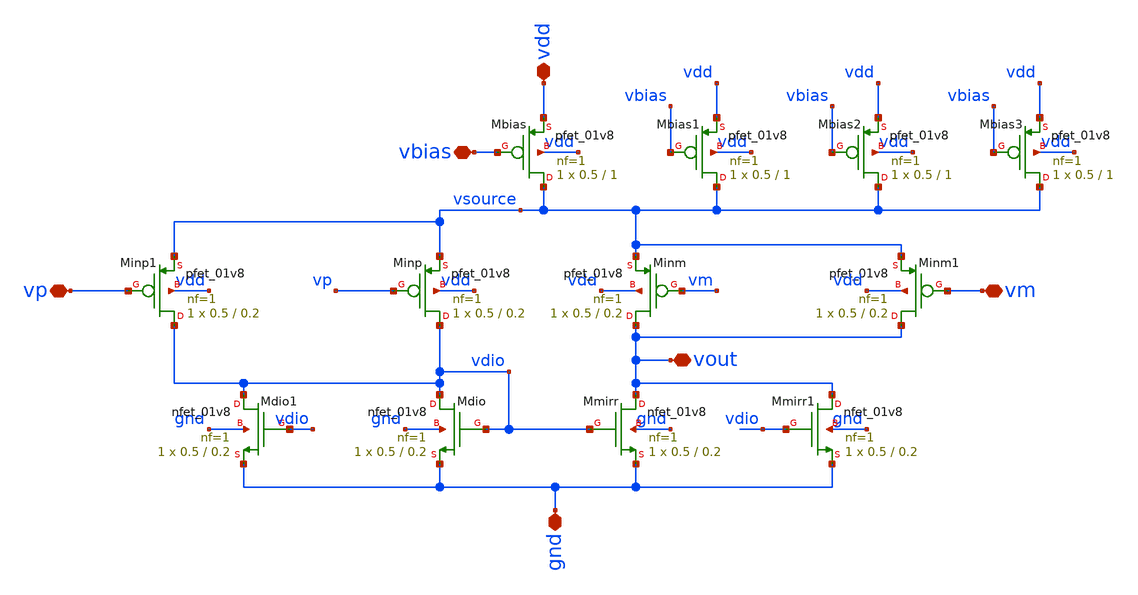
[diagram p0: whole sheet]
** sch_path: analog/xschem/final/col_amp_n_clamp_v1/amp_p_5T.sch
**.subckt amp_p_5T gnd vdd vout vbias vm vp
*.iopin gnd
*.iopin vdd
*.iopin vout
*.iopin vbias
*.iopin vm
*.iopin vp
XMinm vout vm vsource vdd sky130_fd_pr__pfet_01v8 L=0.2 W=0.5 nf=1 ad='int((1 + 1)/2) * 0.5 / 1 * 0.29'
+ as='int((1 + 2)/2) * 0.5 / 1 * 0.29' pd='2*int((1 + 1)/2) * (0.5 / 1 + 0.29)' ps='2*int((1 + 2)/2) * (0.5 / 1 + 0.29)'
+ nrd='0.29 / 0.5 ' nrs='0.29 / 0.5 ' sa=0 sb=0 sd=0 mult=1 m=1
XMinp vdio vp vsource vdd sky130_fd_pr__pfet_01v8 L=0.2 W=0.5 nf=1 ad='int((1 + 1)/2) * 0.5 / 1 * 0.29'
+ as='int((1 + 2)/2) * 0.5 / 1 * 0.29' pd='2*int((1 + 1)/2) * (0.5 / 1 + 0.29)' ps='2*int((1 + 2)/2) * (0.5 / 1 + 0.29)'
+ nrd='0.29 / 0.5 ' nrs='0.29 / 0.5 ' sa=0 sb=0 sd=0 mult=1 m=1
XMdio vdio vdio gnd gnd sky130_fd_pr__nfet_01v8 L=0.2 W=0.5 nf=1 ad='int((1 + 1)/2) * 0.5 / 1 * 0.29'
+ as='int((1 + 2)/2) * 0.5 / 1 * 0.29' pd='2*int((1 + 1)/2) * (0.5 / 1 + 0.29)' ps='2*int((1 + 2)/2) * (0.5 / 1 + 0.29)'
+ nrd='0.29 / 0.5 ' nrs='0.29 / 0.5 ' sa=0 sb=0 sd=0 mult=1 m=1
XMmirr vout vdio gnd gnd sky130_fd_pr__nfet_01v8 L=0.2 W=0.5 nf=1 ad='int((1 + 1)/2) * 0.5 / 1 * 0.29'
+ as='int((1 + 2)/2) * 0.5 / 1 * 0.29' pd='2*int((1 + 1)/2) * (0.5 / 1 + 0.29)' ps='2*int((1 + 2)/2) * (0.5 / 1 + 0.29)'
+ nrd='0.29 / 0.5 ' nrs='0.29 / 0.5 ' sa=0 sb=0 sd=0 mult=1 m=1
XMbias vsource vbias vdd vdd sky130_fd_pr__pfet_01v8 L=1 W=0.5 nf=1 ad='int((1 + 1)/2) * 0.5 / 1 * 0.29'
+ as='int((1 + 2)/2) * 0.5 / 1 * 0.29' pd='2*int((1 + 1)/2) * (0.5 / 1 + 0.29)' ps='2*int((1 + 2)/2) * (0.5 / 1 + 0.29)'
+ nrd='0.29 / 0.5 ' nrs='0.29 / 0.5 ' sa=0 sb=0 sd=0 mult=1 m=1
XMbias1 vsource vbias vdd vdd sky130_fd_pr__pfet_01v8 L=1 W=0.5 nf=1 ad='int((1 + 1)/2) * 0.5 / 1 * 0.29'
+ as='int((1 + 2)/2) * 0.5 / 1 * 0.29' pd='2*int((1 + 1)/2) * (0.5 / 1 + 0.29)' ps='2*int((1 + 2)/2) * (0.5 / 1 + 0.29)'
+ nrd='0.29 / 0.5 ' nrs='0.29 / 0.5 ' sa=0 sb=0 sd=0 mult=1 m=1
XMbias2 vsource vbias vdd vdd sky130_fd_pr__pfet_01v8 L=1 W=0.5 nf=1 ad='int((1 + 1)/2) * 0.5 / 1 * 0.29'
+ as='int((1 + 2)/2) * 0.5 / 1 * 0.29' pd='2*int((1 + 1)/2) * (0.5 / 1 + 0.29)' ps='2*int((1 + 2)/2) * (0.5 / 1 + 0.29)'
+ nrd='0.29 / 0.5 ' nrs='0.29 / 0.5 ' sa=0 sb=0 sd=0 mult=1 m=1
XMbias3 vsource vbias vdd vdd sky130_fd_pr__pfet_01v8 L=1 W=0.5 nf=1 ad='int((1 + 1)/2) * 0.5 / 1 * 0.29'
+ as='int((1 + 2)/2) * 0.5 / 1 * 0.29' pd='2*int((1 + 1)/2) * (0.5 / 1 + 0.29)' ps='2*int((1 + 2)/2) * (0.5 / 1 + 0.29)'
+ nrd='0.29 / 0.5 ' nrs='0.29 / 0.5 ' sa=0 sb=0 sd=0 mult=1 m=1
XMmirr1 vout vdio gnd gnd sky130_fd_pr__nfet_01v8 L=0.2 W=0.5 nf=1 ad='int((1 + 1)/2) * 0.5 / 1 * 0.29'
+ as='int((1 + 2)/2) * 0.5 / 1 * 0.29' pd='2*int((1 + 1)/2) * (0.5 / 1 + 0.29)' ps='2*int((1 + 2)/2) * (0.5 / 1 + 0.29)'
+ nrd='0.29 / 0.5 ' nrs='0.29 / 0.5 ' sa=0 sb=0 sd=0 mult=1 m=1
XMdio1 vdio vdio gnd gnd sky130_fd_pr__nfet_01v8 L=0.2 W=0.5 nf=1 ad='int((1 + 1)/2) * 0.5 / 1 * 0.29'
+ as='int((1 + 2)/2) * 0.5 / 1 * 0.29' pd='2*int((1 + 1)/2) * (0.5 / 1 + 0.29)' ps='2*int((1 + 2)/2) * (0.5 / 1 + 0.29)'
+ nrd='0.29 / 0.5 ' nrs='0.29 / 0.5 ' sa=0 sb=0 sd=0 mult=1 m=1
XMinm1 vout vm vsource vdd sky130_fd_pr__pfet_01v8 L=0.2 W=0.5 nf=1 ad='int((1 + 1)/2) * 0.5 / 1 * 0.29'
+ as='int((1 + 2)/2) * 0.5 / 1 * 0.29' pd='2*int((1 + 1)/2) * (0.5 / 1 + 0.29)' ps='2*int((1 + 2)/2) * (0.5 / 1 + 0.29)'
+ nrd='0.29 / 0.5 ' nrs='0.29 / 0.5 ' sa=0 sb=0 sd=0 mult=1 m=1
XMinp1 vdio vp vsource vdd sky130_fd_pr__pfet_01v8 L=0.2 W=0.5 nf=1 ad='int((1 + 1)/2) * 0.5 / 1 * 0.29'
+ as='int((1 + 2)/2) * 0.5 / 1 * 0.29' pd='2*int((1 + 1)/2) * (0.5 / 1 + 0.29)' ps='2*int((1 + 2)/2) * (0.5 / 1 + 0.29)'
+ nrd='0.29 / 0.5 ' nrs='0.29 / 0.5 ' sa=0 sb=0 sd=0 mult=1 m=1
**.ends
.end
